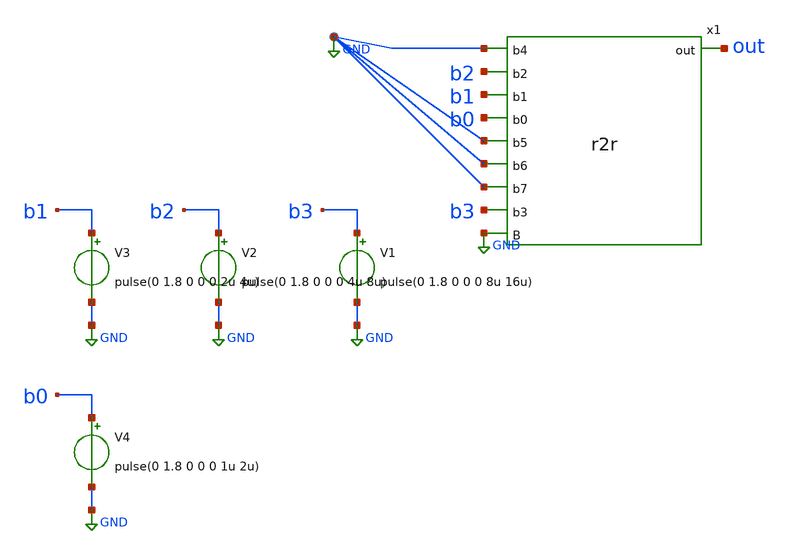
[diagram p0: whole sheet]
** sch_path: xschem/testbench.sch
**.subckt testbench
x1 GND b2 b1 b0 GND GND GND b3 out GND r2r
V1 b3 GND pulse(0 1.8 0 0 0 8u 16u)
V2 b2 GND pulse(0 1.8 0 0 0 4u 8u)
V3 b1 GND pulse(0 1.8 0 0 0 2u 4u)
V4 b0 GND pulse(0 1.8 0 0 0 1u 2u)
**** begin user architecture code

.lib $::SKYWATER_MODELS/sky130.lib.spice tt
.tran 1n 20u uic
.save all

**** end user architecture code
**.ends

* expanding   symbol:  r2r.sym # of pins=10
** sym_path: xschem/r2r.sym
** sch_path: xschem/r2r.sch
.subckt r2r b4 b2 b1 b0 b5 b6 b7 b3 out B
*.ipin b0
*.ipin b1
*.ipin b2
*.ipin b3
*.ipin b4
*.ipin b5
*.ipin b6
*.ipin b7
*.opin out
*.ipin B
XR1 net1 b0 B sky130_fd_pr__res_high_po_0p35 L=1 mult=1 m=1
XR2 net2 b1 B sky130_fd_pr__res_high_po_0p35 L=1 mult=1 m=1
XR3 net3 b2 B sky130_fd_pr__res_high_po_0p35 L=1 mult=1 m=1
XR4 net4 b3 B sky130_fd_pr__res_high_po_0p35 L=1 mult=1 m=1
XR5 net5 b4 B sky130_fd_pr__res_high_po_0p35 L=1 mult=1 m=1
XR6 net6 b5 B sky130_fd_pr__res_high_po_0p35 L=1 mult=1 m=1
XR7 net7 b6 B sky130_fd_pr__res_high_po_0p35 L=1 mult=1 m=1
XR8 out b7 B sky130_fd_pr__res_high_po_0p35 L=1 mult=1 m=1
XR9 net2 net1 B sky130_fd_pr__res_high_po_0p35 L=0.5 mult=1 m=1
XR10 net3 net2 B sky130_fd_pr__res_high_po_0p35 L=0.5 mult=1 m=1
XR11 net4 net3 B sky130_fd_pr__res_high_po_0p35 L=0.5 mult=1 m=1
XR12 net5 net4 B sky130_fd_pr__res_high_po_0p35 L=0.5 mult=1 m=1
XR13 net6 net5 B sky130_fd_pr__res_high_po_0p35 L=0.5 mult=1 m=1
XR14 net7 net6 B sky130_fd_pr__res_high_po_0p35 L=0.5 mult=1 m=1
XR15 out net7 B sky130_fd_pr__res_high_po_0p35 L=0.5 mult=1 m=1
XR16 GND net1 B sky130_fd_pr__res_high_po_0p35 L=1 mult=1 m=1
.ends

.GLOBAL GND
.end
